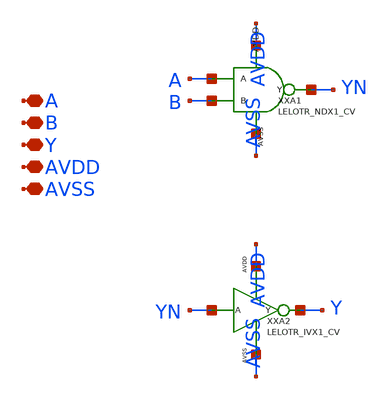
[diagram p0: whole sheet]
** sch_path: design/LELO_TR_GF180MCUD/LELOTR_ANX1_CV.sch
**.subckt LELOTR_ANX1_CV A B Y AVDD AVSS
*.iopin A
*.iopin B
*.iopin Y
*.iopin AVDD
*.iopin AVSS
XXA1 A B YN AVDD AVSS LELOTR_NDX1_CV
XXA2 YN Y AVDD AVSS LELOTR_IVX1_CV
**.ends
.end
